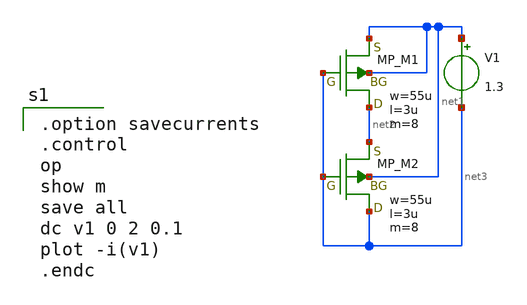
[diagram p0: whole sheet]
** sch_path: member_project/DCDC/xschem/pmos_id_cascode.sch
**.subckt pmos_id_cascode
XM1 net2 net3 net1 net1 PMOS w=55u l=3u as=0 ad=0 ps=0 pd=0 nrd=0 nrs=0 m=8
V1 net1 net3 1.3
XM2 net3 net3 net2 net1 PMOS w=55u l=3u as=0 ad=0 ps=0 pd=0 nrd=0 nrs=0 m=8
**** begin user architecture code
 .include $::LIB/ip62_models

.option savecurrents
.control
op
show m
save all
dc v1 0 2 0.1
plot -i(v1)
.endc

**** end user architecture code
**.ends
.end
